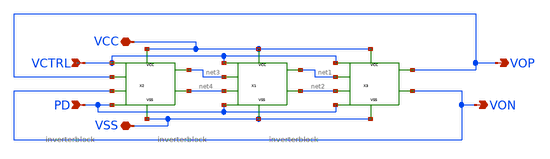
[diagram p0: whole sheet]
** sch_path: xschem/RingOslHw.sch
**.subckt RingOslHw PD VCTRL VCC VSS VON VOP
*.ipin PD
*.ipin VCTRL
*.iopin VCC
*.iopin VSS
*.opin VON
*.opin VOP
X2 VCC VSS net4 net3 VCTRL PD VOP VON inverterblock
X1 VCC VSS net2 net1 VCTRL PD net3 net4 inverterblock
X3 VCC VSS VON VOP VCTRL PD net1 net2 inverterblock
**.ends

* expanding   symbol:  inverterblock.sym # of pins=16
** sym_path: xschem/inverterblock.sym
** sch_path: xschem/inverterblock.sch
.subckt inverterblock VCC VSS VON VOP VCTRL PD VIN VIP
*.ipin VIP
*.opin VON
*.opin VOP
*.ipin PD
*.iopin VSS
*.ipin VIN
*.ipin VCTRL
*.iopin VCC
*.ipin VCTRL
XM9 net1 PD VSS VSS sky130_fd_pr__nfet_01v8 L=0.15 W=1 nf=1 ad='int((nf+1)/2) * W/nf * 0.29' as='int((nf+2)/2) * W/nf * 0.29'
+ pd='2*int((nf+1)/2) * (W/nf + 0.29)' ps='2*int((nf+2)/2) * (W/nf + 0.29)' nrd='0.29 / W' nrs='0.29 / W'
+ sa=0 sb=0 sd=0 mult=1 m=1
XM10 VON VCTRL VCC VCC sky130_fd_pr__pfet_01v8 L=0.15 W=1 nf=1 ad='int((nf+1)/2) * W/nf * 0.29' as='int((nf+2)/2) * W/nf * 0.29'
+ pd='2*int((nf+1)/2) * (W/nf + 0.29)' ps='2*int((nf+2)/2) * (W/nf + 0.29)' nrd='0.29 / W' nrs='0.29 / W'
+ sa=0 sb=0 sd=0 mult=1 m=1
XM3 VON VOP VCC VCC sky130_fd_pr__pfet_01v8 L=0.15 W=1 nf=1 ad='int((nf+1)/2) * W/nf * 0.29' as='int((nf+2)/2) * W/nf * 0.29'
+ pd='2*int((nf+1)/2) * (W/nf + 0.29)' ps='2*int((nf+2)/2) * (W/nf + 0.29)' nrd='0.29 / W' nrs='0.29 / W'
+ sa=0 sb=0 sd=0 mult=1 m=1
XM4 VOP VON VCC VCC sky130_fd_pr__pfet_01v8 L=0.15 W=1 nf=1 ad='int((nf+1)/2) * W/nf * 0.29' as='int((nf+2)/2) * W/nf * 0.29'
+ pd='2*int((nf+1)/2) * (W/nf + 0.29)' ps='2*int((nf+2)/2) * (W/nf + 0.29)' nrd='0.29 / W' nrs='0.29 / W'
+ sa=0 sb=0 sd=0 mult=1 m=1
XM5 VOP VCTRL VCC VCC sky130_fd_pr__pfet_01v8 L=0.15 W=1 nf=1 ad='int((nf+1)/2) * W/nf * 0.29' as='int((nf+2)/2) * W/nf * 0.29'
+ pd='2*int((nf+1)/2) * (W/nf + 0.29)' ps='2*int((nf+2)/2) * (W/nf + 0.29)' nrd='0.29 / W' nrs='0.29 / W'
+ sa=0 sb=0 sd=0 mult=1 m=1
XM6 VON VIP net1 VSS sky130_fd_pr__nfet_01v8 L=0.15 W=1 nf=1 ad='int((nf+1)/2) * W/nf * 0.29' as='int((nf+2)/2) * W/nf * 0.29'
+ pd='2*int((nf+1)/2) * (W/nf + 0.29)' ps='2*int((nf+2)/2) * (W/nf + 0.29)' nrd='0.29 / W' nrs='0.29 / W'
+ sa=0 sb=0 sd=0 mult=1 m=1
XM7 VOP VIN net1 VSS sky130_fd_pr__nfet_01v8 L=0.15 W=1 nf=1 ad='int((nf+1)/2) * W/nf * 0.29' as='int((nf+2)/2) * W/nf * 0.29'
+ pd='2*int((nf+1)/2) * (W/nf + 0.29)' ps='2*int((nf+2)/2) * (W/nf + 0.29)' nrd='0.29 / W' nrs='0.29 / W'
+ sa=0 sb=0 sd=0 mult=1 m=1
.ends

.end
